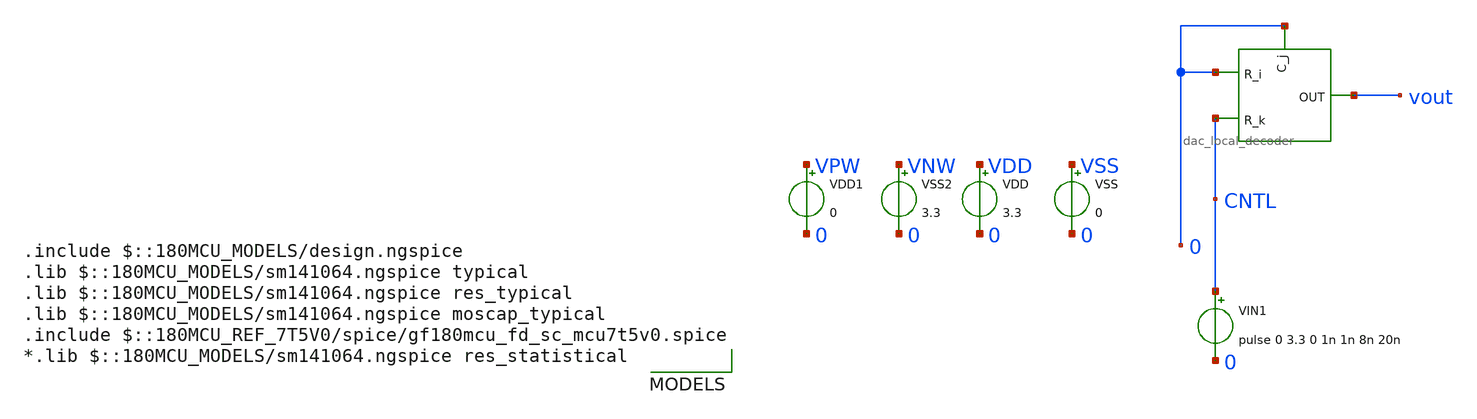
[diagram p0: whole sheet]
** sch_path: DAC/xschem/digital_cell/tb_files/test_dac_local_decoder.sch
**.subckt test_dac_local_decoder
VIN1 CNTL 0 pulse 0 3.3 0 1n 1n 8n 20n
VDD VDD 0 3.3
VSS VSS 0 0
VDD1 VPW 0 0
VSS2 VNW 0 3.3
x1 0 CNTL 0 vout VDD VNW VPW VSS dac_local_decoder
**** begin user architecture code

.include $::180MCU_MODELS/design.ngspice
.lib $::180MCU_MODELS/sm141064.ngspice typical
.lib $::180MCU_MODELS/sm141064.ngspice res_typical
.lib $::180MCU_MODELS/sm141064.ngspice moscap_typical
.include $::180MCU_REF_7T5V0/spice/gf180mcu_fd_sc_mcu7t5v0.spice
*.lib $::180MCU_MODELS/sm141064.ngspice res_statistical





.control
	tran 0.1n 50n
	plot v(CNTL) V(vout)
	plot v(vout)
	write test_dac_local_decoder.raw

.endc
.save all




**** end user architecture code
**.ends
.end
